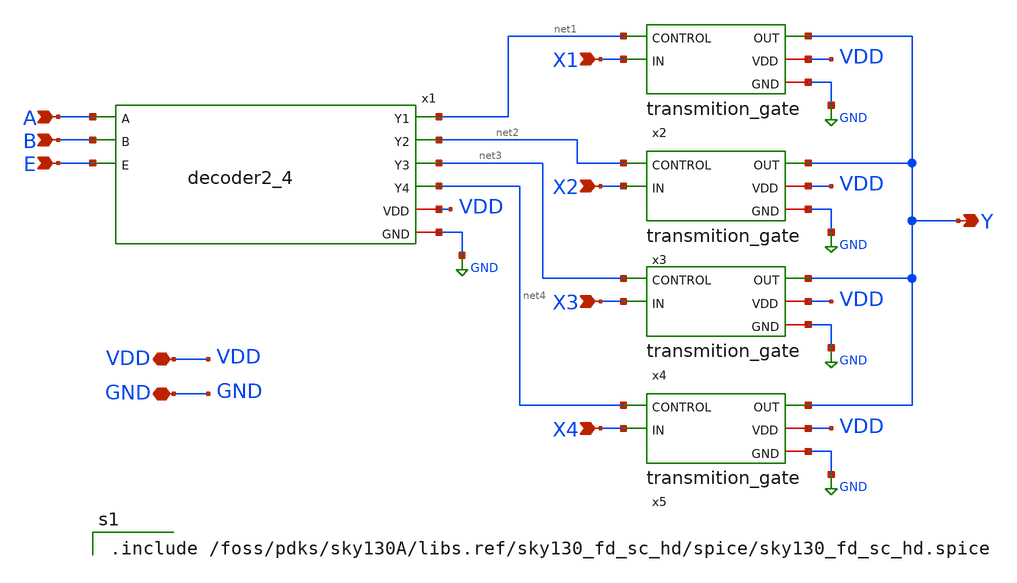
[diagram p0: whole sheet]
** sch_path: src/analog_source_files/amux4.sch
**.subckt amux4 VDD GND Y A B E X1 X2 X3 X4
*.iopin VDD
*.iopin GND
*.opin Y
*.ipin A
*.ipin B
*.ipin E
*.ipin X1
*.ipin X2
*.ipin X3
*.ipin X4
x2 net1 Y X1 VDD GND transmition_gate
x3 net2 Y X2 VDD GND transmition_gate
x4 net3 Y X3 VDD GND transmition_gate
x5 net4 Y X4 VDD GND transmition_gate
x1 A B net1 net2 net3 net4 E VDD GND decoder2_4
**** begin user architecture code

.include /foss/pdks/sky130A/libs.ref/sky130_fd_sc_hd/spice/sky130_fd_sc_hd.spice


**** end user architecture code
**.ends

* expanding   symbol:  transmition_gate.sym # of pins=5
** sym_path: src/analog_source_files/transmition_gate.sym
** sch_path: src/analog_source_files/transmition_gate.sch
.subckt transmition_gate CONTROL OUT IN VDD GND
*.ipin IN
*.ipin CONTROL
*.opin OUT
*.iopin VDD
*.iopin GND
XM2 IN net1 OUT VDD sky130_fd_pr__pfet_01v8 L=0.15 W=1 nf=1 ad='int((1 + 1)/2) * 1 / 1 * 0.29' as='int((1 + 2)/2) * 1 / 1 * 0.29'
+ pd='2*int((1 + 1)/2) * (1 / 1 + 0.29)' ps='2*int((1 + 2)/2) * (1 / 1 + 0.29)' nrd='0.29 / 1 ' nrs='0.29 / 1 '
+ sa=0 sb=0 sd=0 mult=1 m=1
x1 CONTROL GND GND VDD VDD net1 sky130_fd_sc_hd__inv_1
XM3 IN CONTROL OUT GND sky130_fd_pr__nfet_01v8 L=0.15 W=1 nf=1 ad='int((1 + 1)/2) * 1 / 1 * 0.29' as='int((1 + 2)/2) * 1 / 1 * 0.29'
+ pd='2*int((1 + 1)/2) * (1 / 1 + 0.29)' ps='2*int((1 + 2)/2) * (1 / 1 + 0.29)' nrd='0.29 / 1 ' nrs='0.29 / 1 '
+ sa=0 sb=0 sd=0 mult=1 m=1
.ends


* expanding   symbol:  decoder2_4.sym # of pins=9
** sym_path: src/analog_source_files/decoder2_4.sym
** sch_path: src/analog_source_files/decoder2_4.sch
.subckt decoder2_4 A B Y1 Y2 Y3 Y4 E VDD GND
*.ipin E
*.ipin B
*.ipin A
*.opin Y1
*.opin Y2
*.opin Y3
*.opin Y4
*.iopin VDD
*.iopin GND
x1 net1 net2 E GND GND VDD VDD Y1 sky130_fd_sc_hd__and3_2
x2 A net2 E GND GND VDD VDD Y2 sky130_fd_sc_hd__and3_2
x3 net1 B E GND GND VDD VDD Y3 sky130_fd_sc_hd__and3_2
x4 A B E GND GND VDD VDD Y4 sky130_fd_sc_hd__and3_2
x5 A GND GND VDD VDD net1 sky130_fd_sc_hd__inv_1
x6 B GND GND VDD VDD net2 sky130_fd_sc_hd__inv_1
.ends

.GLOBAL GND
.end
